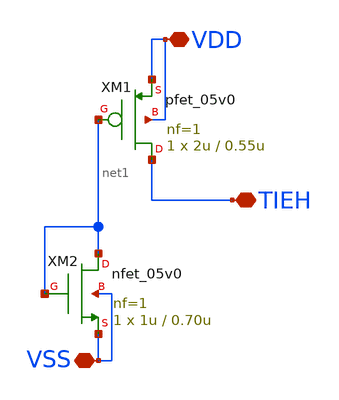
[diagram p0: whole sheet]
** sch_path: blocks/composite/regulated_cascoded_cmirror/xschem/Chipathon2025_pads/xschem/tieH.sch
**.subckt tieH VSS VDD TIEH
*.iopin VSS
*.iopin VDD
*.iopin TIEH
XM1 TIEH net1 VDD VDD pfet_05v0 L=0.55u W=2u nf=1 ad='int((nf+1)/2) * W/nf * 0.18u' as='int((nf+2)/2) * W/nf * 0.18u'
+ pd='2*int((nf+1)/2) * (W/nf + 0.18u)' ps='2*int((nf+2)/2) * (W/nf + 0.18u)' nrd='0.18u / W' nrs='0.18u / W'
+ sa=0 sb=0 sd=0 m=1
XM2 net1 net1 VSS VSS nfet_05v0 L=0.70u W=1u nf=1 ad='int((nf+1)/2) * W/nf * 0.18u' as='int((nf+2)/2) * W/nf * 0.18u'
+ pd='2*int((nf+1)/2) * (W/nf + 0.18u)' ps='2*int((nf+2)/2) * (W/nf + 0.18u)' nrd='0.18u / W' nrs='0.18u / W'
+ sa=0 sb=0 sd=0 m=1
**.ends
.end
